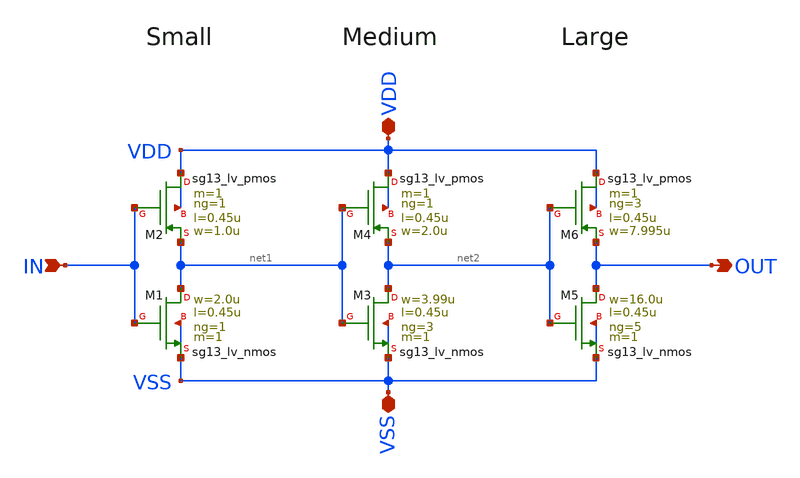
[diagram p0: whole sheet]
** sch_path: TSENSE8490-main/schematic/xschem/lvs-view/analog/buffer/buffer.sch
**.subckt buffer IN OUT VSS VDD
*.ipin IN
*.opin OUT
*.iopin VSS
*.iopin VDD
XM1 net1 IN VSS VSS sg13_lv_nmos w=2.0u l=0.45u ng=1 m=1 mm_ok=1
XM2 VDD IN net1 VDD sg13_lv_pmos w=1.0u l=0.45u ng=1 m=1 mm_ok=1
XM3 net2 net1 VSS VSS sg13_lv_nmos w=3.99u l=0.45u ng=3 m=1 mm_ok=1
XM4 VDD net1 net2 VDD sg13_lv_pmos w=2.0u l=0.45u ng=1 m=1 mm_ok=1
XM5 OUT net2 VSS VSS sg13_lv_nmos w=16.0u l=0.45u ng=5 m=1 mm_ok=1
XM6 VDD net2 OUT VDD sg13_lv_pmos w=7.995u l=0.45u ng=3 m=1 mm_ok=1
**.ends
.end
